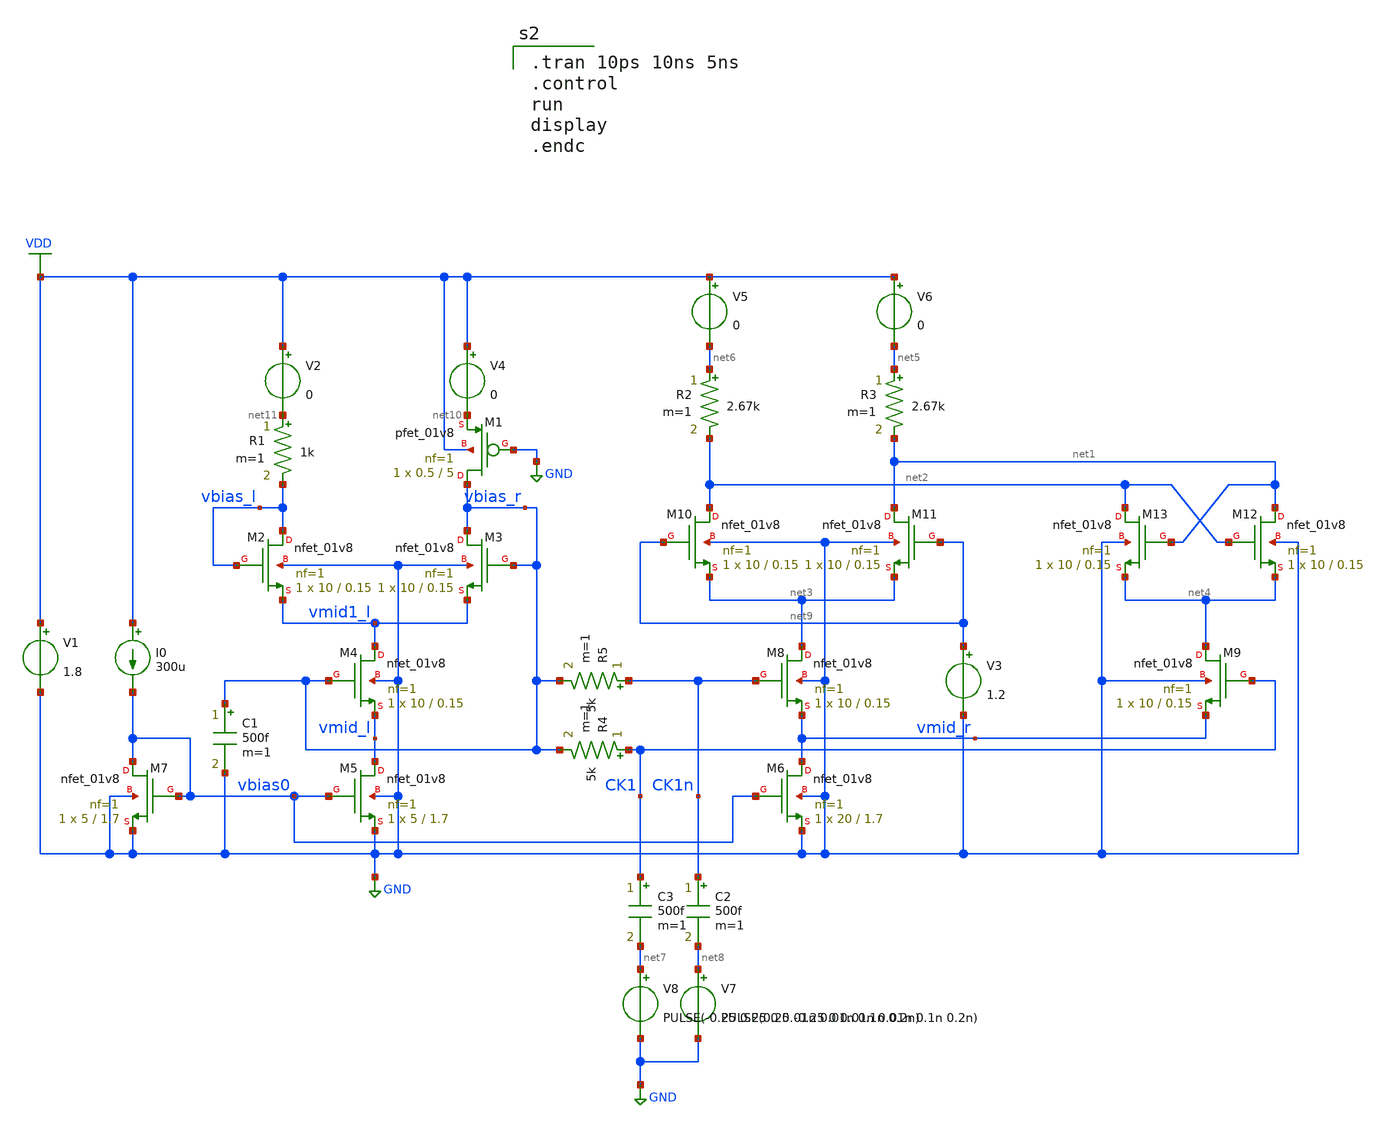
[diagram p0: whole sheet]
** sch_path: xschem/bias_replica.sch
**.subckt bias_replica
XM1 vbias_r GND net10 VDD sky130_fd_pr__pfet_01v8 L=5 W=0.5 nf=1 ad='int((nf+1)/2) * W/nf * 0.29' as='int((nf+2)/2) * W/nf * 0.29'
+ pd='2*int((nf+1)/2) * (W/nf + 0.29)' ps='2*int((nf+2)/2) * (W/nf + 0.29)' nrd='0.29 / W' nrs='0.29 / W'
+ sa=0 sb=0 sd=0 mult=1 m=1
XM2 vbias_l vbias_l vmid1_l GND sky130_fd_pr__nfet_01v8 L=0.15 W=10 nf=1 ad='int((nf+1)/2) * W/nf * 0.29'
+ as='int((nf+2)/2) * W/nf * 0.29' pd='2*int((nf+1)/2) * (W/nf + 0.29)' ps='2*int((nf+2)/2) * (W/nf + 0.29)'
+ nrd='0.29 / W' nrs='0.29 / W' sa=0 sb=0 sd=0 mult=1 m=1
XM3 vbias_r vbias_r vmid1_l GND sky130_fd_pr__nfet_01v8 L=0.15 W=10 nf=1 ad='int((nf+1)/2) * W/nf * 0.29'
+ as='int((nf+2)/2) * W/nf * 0.29' pd='2*int((nf+1)/2) * (W/nf + 0.29)' ps='2*int((nf+2)/2) * (W/nf + 0.29)'
+ nrd='0.29 / W' nrs='0.29 / W' sa=0 sb=0 sd=0 mult=1 m=1
XM4 vmid1_l vbias_r vmid_l GND sky130_fd_pr__nfet_01v8 L=0.15 W=10 nf=1 ad='int((nf+1)/2) * W/nf * 0.29'
+ as='int((nf+2)/2) * W/nf * 0.29' pd='2*int((nf+1)/2) * (W/nf + 0.29)' ps='2*int((nf+2)/2) * (W/nf + 0.29)'
+ nrd='0.29 / W' nrs='0.29 / W' sa=0 sb=0 sd=0 mult=1 m=1
XM5 vmid_l vbias0 GND GND sky130_fd_pr__nfet_01v8 L=1.7 W=5 nf=1 ad='int((nf+1)/2) * W/nf * 0.29' as='int((nf+2)/2) * W/nf * 0.29'
+ pd='2*int((nf+1)/2) * (W/nf + 0.29)' ps='2*int((nf+2)/2) * (W/nf + 0.29)' nrd='0.29 / W' nrs='0.29 / W'
+ sa=0 sb=0 sd=0 mult=1 m=1
R1 net11 vbias_l 1k m=1
C1 vbias_r GND 500f m=1
XM6 vmid_r vbias0 GND GND sky130_fd_pr__nfet_01v8 L=1.7 W=20 nf=1 ad='int((nf+1)/2) * W/nf * 0.29' as='int((nf+2)/2) * W/nf * 0.29'
+ pd='2*int((nf+1)/2) * (W/nf + 0.29)' ps='2*int((nf+2)/2) * (W/nf + 0.29)' nrd='0.29 / W' nrs='0.29 / W'
+ sa=0 sb=0 sd=0 mult=1 m=1
XM7 vbias0 vbias0 GND GND sky130_fd_pr__nfet_01v8 L=1.7 W=5 nf=1 ad='int((nf+1)/2) * W/nf * 0.29' as='int((nf+2)/2) * W/nf * 0.29'
+ pd='2*int((nf+1)/2) * (W/nf + 0.29)' ps='2*int((nf+2)/2) * (W/nf + 0.29)' nrd='0.29 / W' nrs='0.29 / W'
+ sa=0 sb=0 sd=0 mult=1 m=1
I0 VDD vbias0 300u
V1 VDD GND 1.8
XM8 net3 CK1n vmid_r GND sky130_fd_pr__nfet_01v8 L=0.15 W=10 nf=1 ad='int((nf+1)/2) * W/nf * 0.29' as='int((nf+2)/2) * W/nf * 0.29'
+ pd='2*int((nf+1)/2) * (W/nf + 0.29)' ps='2*int((nf+2)/2) * (W/nf + 0.29)' nrd='0.29 / W' nrs='0.29 / W'
+ sa=0 sb=0 sd=0 mult=1 m=1
XM9 net4 CK1 vmid_r GND sky130_fd_pr__nfet_01v8 L=0.15 W=10 nf=1 ad='int((nf+1)/2) * W/nf * 0.29' as='int((nf+2)/2) * W/nf * 0.29'
+ pd='2*int((nf+1)/2) * (W/nf + 0.29)' ps='2*int((nf+2)/2) * (W/nf + 0.29)' nrd='0.29 / W' nrs='0.29 / W'
+ sa=0 sb=0 sd=0 mult=1 m=1
XM10 net2 net9 net3 GND sky130_fd_pr__nfet_01v8 L=0.15 W=10 nf=1 ad='int((nf+1)/2) * W/nf * 0.29' as='int((nf+2)/2) * W/nf * 0.29'
+ pd='2*int((nf+1)/2) * (W/nf + 0.29)' ps='2*int((nf+2)/2) * (W/nf + 0.29)' nrd='0.29 / W' nrs='0.29 / W'
+ sa=0 sb=0 sd=0 mult=1 m=1
XM11 net1 net9 net3 GND sky130_fd_pr__nfet_01v8 L=0.15 W=10 nf=1 ad='int((nf+1)/2) * W/nf * 0.29' as='int((nf+2)/2) * W/nf * 0.29'
+ pd='2*int((nf+1)/2) * (W/nf + 0.29)' ps='2*int((nf+2)/2) * (W/nf + 0.29)' nrd='0.29 / W' nrs='0.29 / W'
+ sa=0 sb=0 sd=0 mult=1 m=1
XM12 net1 net2 net4 GND sky130_fd_pr__nfet_01v8 L=0.15 W=10 nf=1 ad='int((nf+1)/2) * W/nf * 0.29' as='int((nf+2)/2) * W/nf * 0.29'
+ pd='2*int((nf+1)/2) * (W/nf + 0.29)' ps='2*int((nf+2)/2) * (W/nf + 0.29)' nrd='0.29 / W' nrs='0.29 / W'
+ sa=0 sb=0 sd=0 mult=1 m=1
XM13 net2 net1 net4 GND sky130_fd_pr__nfet_01v8 L=0.15 W=10 nf=1 ad='int((nf+1)/2) * W/nf * 0.29' as='int((nf+2)/2) * W/nf * 0.29'
+ pd='2*int((nf+1)/2) * (W/nf + 0.29)' ps='2*int((nf+2)/2) * (W/nf + 0.29)' nrd='0.29 / W' nrs='0.29 / W'
+ sa=0 sb=0 sd=0 mult=1 m=1
R2 net6 net2 2.67k m=1
R3 net5 net1 2.67k m=1
R4 CK1 vbias_r 5k m=1
R5 CK1n vbias_r 5k m=1
C2 CK1n net8 500f m=1
C3 CK1 net7 500f m=1
V3 net9 GND 1.2
V2 VDD net11 0
V4 VDD net10 0
V5 VDD net6 0
V6 VDD net5 0
V8 net7 GND PULSE(-0.25 0.25 0 0.01n 0.01n 0.1n 0.2n)
V7 net8 GND PULSE(0.25 -0.25 0 0.01n 0.01n 0.1n 0.2n)
**** begin user architecture code

.tran 10ps 10ns 5ns
.control
run
display
.endc


.lib $::SKYWATER_MODELS/sky130.lib.spice tt
.include $::PDKPATH/libs.ref/sky130_fd_sc_hs/spice/sky130_fd_sc_hs.spice

**** end user architecture code
**.ends
.GLOBAL GND
.GLOBAL VDD
.end
